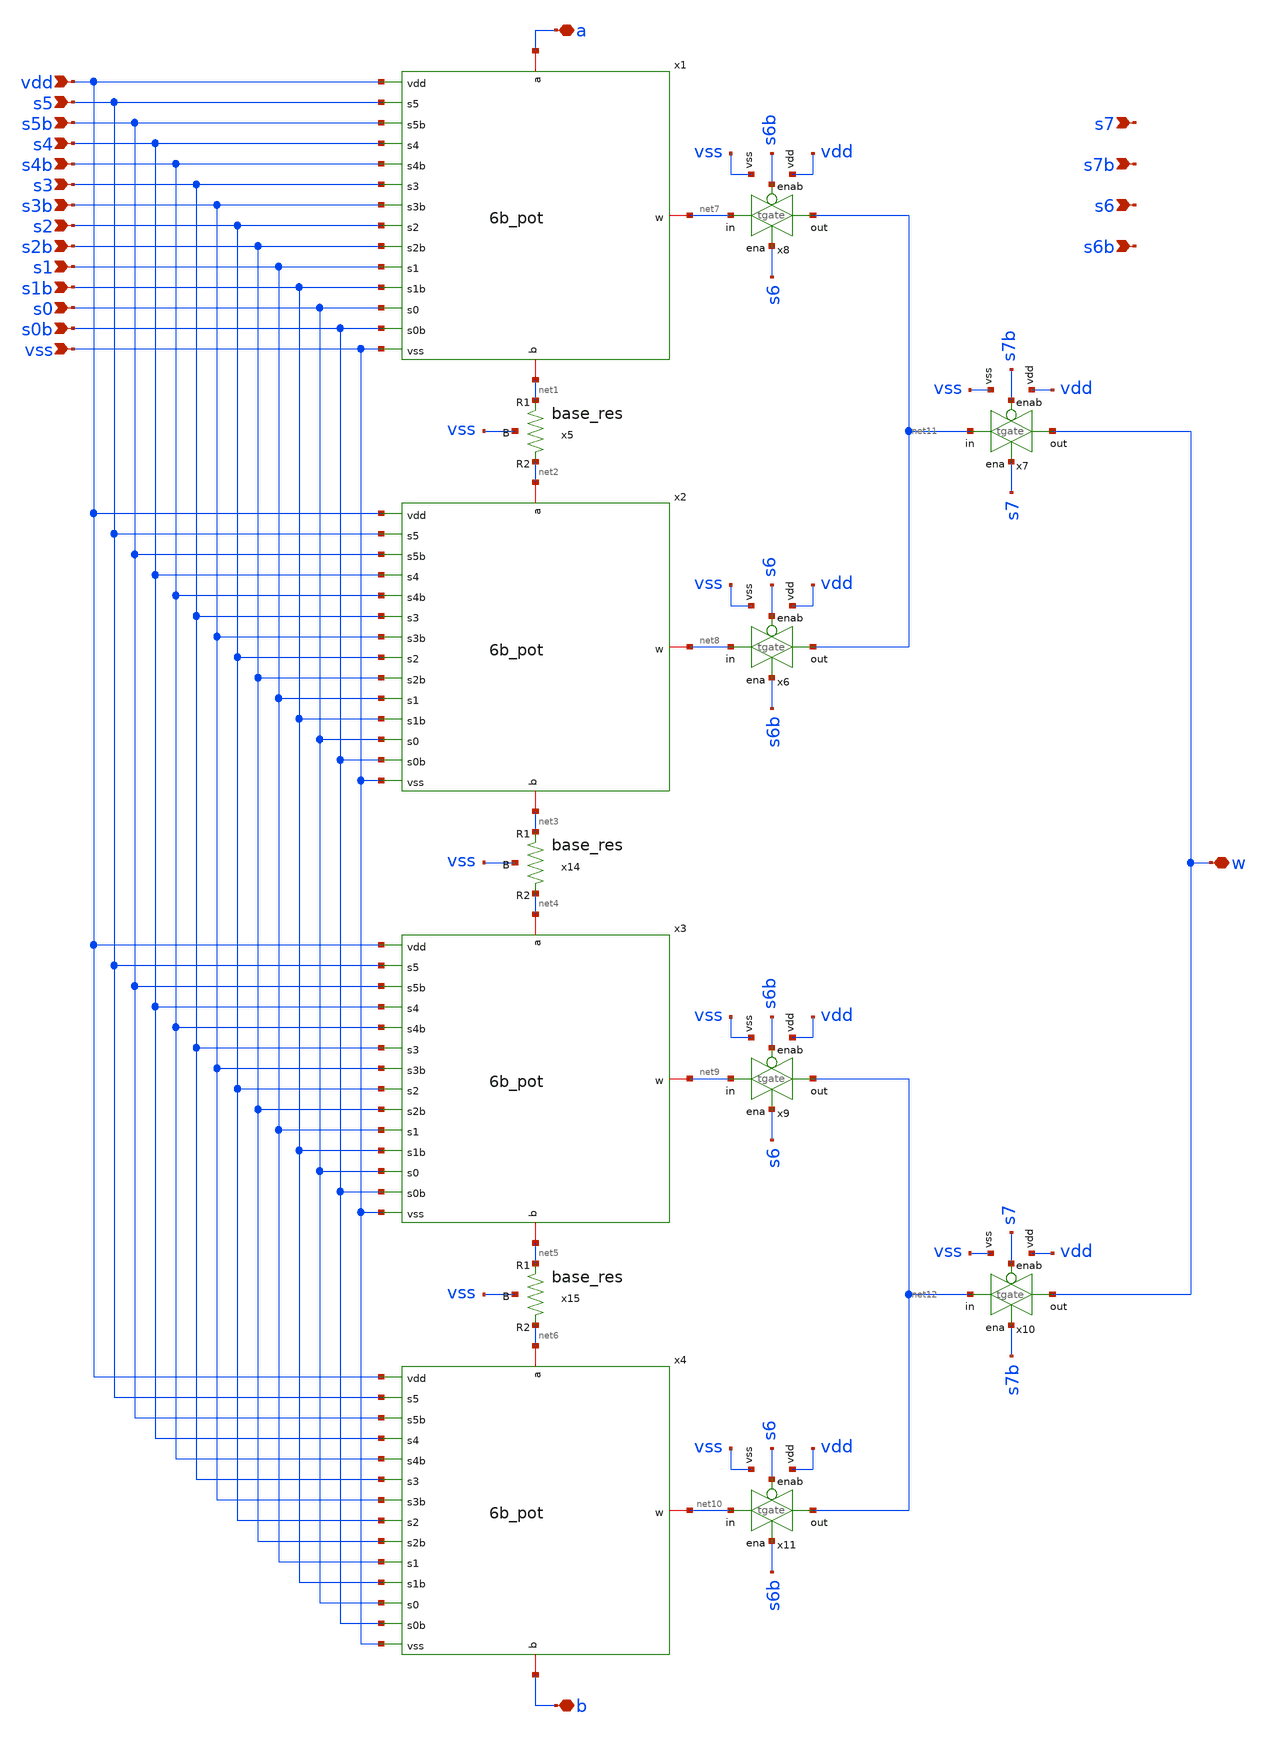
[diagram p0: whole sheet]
** sch_path: xschem/8b_pot.sch
**.subckt 8b_pot s0 s0b s1 s1b s2 s2b s3 s3b s4 s4b s5 s5b s6 s6b s7 s7b vss vdd a w b
*.ipin s0
*.ipin s0b
*.ipin s1
*.ipin s1b
*.ipin s2
*.ipin s2b
*.ipin s3
*.ipin s3b
*.ipin s4
*.ipin s4b
*.ipin s5
*.ipin s5b
*.ipin s6
*.ipin s6b
*.ipin s7
*.ipin s7b
*.ipin vss
*.ipin vdd
*.iopin a
*.iopin w
*.iopin b
x1 vdd s5 s5b s4 s4b a s3 net7 s3b s2 s2b s1 s1b s0 s0b vss net1 6b_pot
x2 vdd s5 s5b s4 s4b net2 s3 net8 s3b s2 s2b s1 s1b s0 s0b vss net3 6b_pot
x3 vdd s5 s5b s4 s4b net4 s3 net9 s3b s2 s2b s1 s1b s0 s0b vss net5 6b_pot
x4 vdd s5 s5b s4 s4b net6 s3 net10 s3b s2 s2b s1 s1b s0 s0b vss b 6b_pot
x5 net1 net2 vss base_res
x14 net3 net4 vss base_res
x15 net5 net6 vss base_res
x8 vdd s6b net7 net11 s6 vss tgate
x6 vdd s6 net8 net11 s6b vss tgate
x7 vdd s7b net11 w s7 vss tgate
x9 vdd s6b net9 net12 s6 vss tgate
x10 vdd s7 net12 w s7b vss tgate
x11 vdd s6 net10 net12 s6b vss tgate
**.ends

* expanding   symbol:  xschem/6b_pot.sym # of pins=17
** sym_path: xschem/6b_pot.sym
** sch_path: xschem/6b_pot.sch
.subckt 6b_pot vdd s5 s5b s4 s4b a s3 w s3b s2 s2b s1 s1b s0 s0b vss b
*.ipin s0
*.ipin s0b
*.ipin s1
*.ipin s1b
*.ipin s2
*.ipin s2b
*.ipin s3
*.ipin s3b
*.ipin s4
*.ipin s4b
*.ipin s5
*.ipin s5b
*.ipin vss
*.ipin vdd
*.iopin a
*.iopin w
*.iopin b
x1 vdd a s3 s3b s2 s2b net10 s1 s1b s0 s0b net2 vss 4b_pot
x2 vdd net1 s3 s3b s2 s2b net9 s1 s1b s0 s0b net4 vss 4b_pot
x3 vdd net3 s3 s3b s2 s2b net8 s1 s1b s0 s0b net6 vss 4b_pot
x4 vdd net5 s3 s3b s2 s2b net7 s1 s1b s0 s0b b vss 4b_pot
x9 net2 net1 vss base_res
x10 net4 net3 vss base_res
x11 net6 net5 vss base_res
x8 vdd s4b net10 net12 s4 vss tgate
x5 vdd s5b net12 w s5 vss tgate
x6 vdd s4 net9 net12 s4b vss tgate
x7 vdd s4b net8 net11 s4 vss tgate
x12 vdd s4 net7 net11 s4b vss tgate
x13 vdd s5 net11 w s5b vss tgate
.ends


* expanding   symbol:  xschem/base_res.sym # of pins=3
** sym_path: xschem/base_res.sym
** sch_path: xschem/base_res.sch
.subckt base_res R1 R2 B
*.iopin R1
*.iopin R2
*.iopin B
XR2 R2 R1 B sky130_fd_pr__res_high_po_2p85 L=0.57 mult=1 m=1
.ends


* expanding   symbol:  xschem/tgate.sym # of pins=6
** sym_path: xschem/tgate.sym
** sch_path: xschem/tgate.sch
.subckt tgate vdd enab in out ena vss
*.ipin enab
*.ipin ena
*.ipin in
*.opin out
*.iopin vdd
*.iopin vss
XMn out ena in vss sky130_fd_pr__nfet_g5v0d10v5 L=0.5 W=80 nf=4 ad='int((nf+1)/2) * W/nf * 0.29' as='int((nf+2)/2) * W/nf * 0.29'
+ pd='2*int((nf+1)/2) * (W/nf + 0.29)' ps='2*int((nf+2)/2) * (W/nf + 0.29)' nrd='0.29 / W' nrs='0.29 / W'
+ sa=0 sb=0 sd=0 mult=1 m=1
XMp out enab in vdd sky130_fd_pr__pfet_g5v0d10v5 L=0.5 W=80 nf=4 ad='int((nf+1)/2) * W/nf * 0.29' as='int((nf+2)/2) * W/nf * 0.29'
+ pd='2*int((nf+1)/2) * (W/nf + 0.29)' ps='2*int((nf+2)/2) * (W/nf + 0.29)' nrd='0.29 / W' nrs='0.29 / W'
+ sa=0 sb=0 sd=0 mult=1 m=1
.ends


* expanding   symbol:  xschem/4b_pot.sym # of pins=13
** sym_path: xschem/4b_pot.sym
** sch_path: xschem/4b_pot.sch
.subckt 4b_pot vdd a s3 s3b s2 s2b w s1 s1b s0 s0b b vss
*.ipin s0
*.ipin s0b
*.ipin s1
*.ipin s1b
*.ipin s2
*.ipin s2b
*.ipin s3
*.ipin s3b
*.ipin vss
*.ipin vdd
*.iopin a
*.iopin w
*.iopin b
x9 net7 net8 vss base_res
x1 vdd a s1 s1b net4 s0 s0b net7 vss 2b_pot
x2 vdd net8 s1 s1b net3 s0 s0b net9 vss 2b_pot
x3 vdd net10 s1 s1b net2 s0 s0b net11 vss 2b_pot
x4 vdd net12 s1 s1b net1 s0 s0b b vss 2b_pot
x5 net9 net10 vss base_res
x6 net11 net12 vss base_res
x8 vdd s2b net4 net6 s2 vss tgate
x7 vdd s2 net3 net6 s2b vss tgate
x10 vdd s2b net2 net5 s2 vss tgate
x11 vdd s2 net1 net5 s2b vss tgate
x12 vdd s3 net5 w s3b vss tgate
x13 vdd s3b net6 w s3 vss tgate
.ends


* expanding   symbol:  xschem/2b_pot.sym # of pins=9
** sym_path: xschem/2b_pot.sym
** sch_path: xschem/2b_pot.sch
.subckt 2b_pot vdd a s1 s1b w s0 s0b b vss
*.ipin s0
*.ipin s0b
*.ipin s1
*.ipin vss
*.ipin vdd
*.iopin a
*.iopin w
*.iopin b
*.ipin s1b
x1 vdd a net4 s0b s0 net1 vss 1b_pot
x2 vdd net2 net3 s0b s0 b vss 1b_pot
x5 net1 net2 vss base_res
x8 vdd s1b net4 w s1 vss tgate
x3 vdd s1 net3 w s1b vss tgate
.ends


* expanding   symbol:  xschem/1b_pot.sym # of pins=7
** sym_path: xschem/1b_pot.sym
** sch_path: xschem/1b_pot.sch
.subckt 1b_pot vdd a w s0b s0 b vss
*.ipin s0
*.ipin s0b
*.ipin vdd
*.ipin vss
*.ipin a
*.ipin b
*.opin w
x1 a b vss base_res
x2 vdd s0b a w s0 vss tgate
x3 vdd s0 b w s0b vss tgate
.ends

.end
